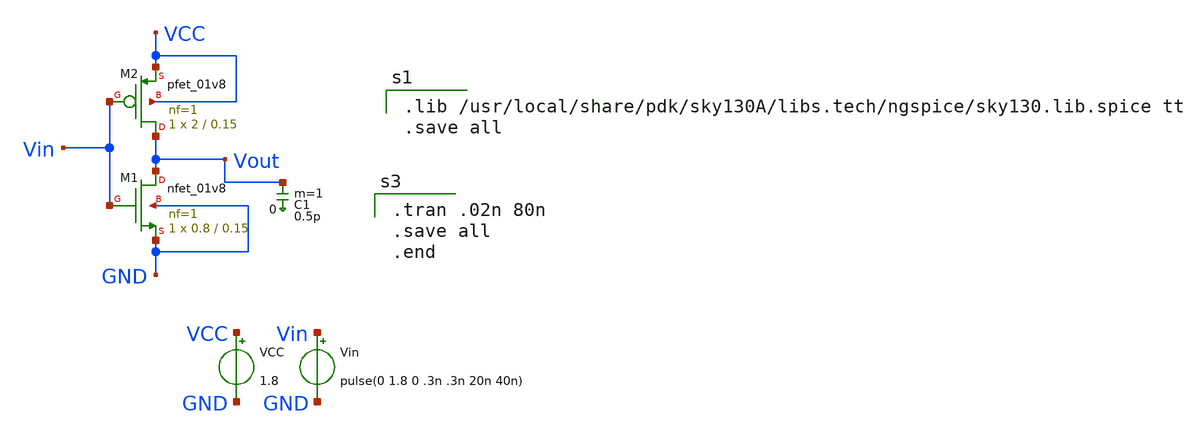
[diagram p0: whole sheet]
** sch_path: Schematic/cmos_inv_schematic.sch
**.subckt cmos_inv_schematic
VCC VCC GND 1.8
Vin Vin GND pulse(0 1.8 0 .3n .3n 20n 40n)
XM1 Vout Vin GND GND sky130_fd_pr__nfet_01v8 L=0.15 W=0.8 nf=1 ad='int((nf+1)/2) * W/nf * 0.29' as='int((nf+2)/2) * W/nf * 0.29'
+ pd='2*int((nf+1)/2) * (W/nf + 0.29)' ps='2*int((nf+2)/2) * (W/nf + 0.29)' nrd='0.29 / W' nrs='0.29 / W'
+ sa=0 sb=0 sd=0 mult=1 m=1
XM2 Vout Vin VCC VCC sky130_fd_pr__pfet_01v8 L=0.15 W=2 nf=1 ad='int((nf+1)/2) * W/nf * 0.29' as='int((nf+2)/2) * W/nf * 0.29'
+ pd='2*int((nf+1)/2) * (W/nf + 0.29)' ps='2*int((nf+2)/2) * (W/nf + 0.29)' nrd='0.29 / W' nrs='0.29 / W'
+ sa=0 sb=0 sd=0 mult=1 m=1
C1 Vout 0 0.5p m=1
**** begin user architecture code

.lib /usr/local/share/pdk/sky130A/libs.tech/ngspice/sky130.lib.spice tt
.save all


.tran .02n 80n
.save all
.end

**** end user architecture code
**.ends
.end
